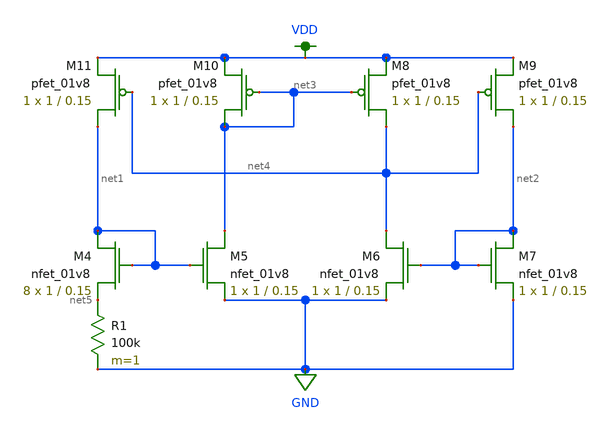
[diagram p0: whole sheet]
** sch_path: current_bias.sch
**.subckt current_bias
XM4 net1 net1 net5 GND sky130_fd_pr__nfet_01v8 L=0.15 W=1 nf=1 ad='int((nf+1)/2) * W/nf * 0.29' as='int((nf+2)/2) * W/nf * 0.29'
+ pd='2*int((nf+1)/2) * (W/nf + 0.29)' ps='2*int((nf+2)/2) * (W/nf + 0.29)' nrd='0.29 / W' nrs='0.29 / W'
+ sa=0 sb=0 sd=0 mult=8 m=8
XM5 net3 net1 GND GND sky130_fd_pr__nfet_01v8 L=0.15 W=1 nf=1 ad='int((nf+1)/2) * W/nf * 0.29' as='int((nf+2)/2) * W/nf * 0.29'
+ pd='2*int((nf+1)/2) * (W/nf + 0.29)' ps='2*int((nf+2)/2) * (W/nf + 0.29)' nrd='0.29 / W' nrs='0.29 / W'
+ sa=0 sb=0 sd=0 mult=1 m=1
XM6 net4 net2 GND GND sky130_fd_pr__nfet_01v8 L=0.15 W=1 nf=1 ad='int((nf+1)/2) * W/nf * 0.29' as='int((nf+2)/2) * W/nf * 0.29'
+ pd='2*int((nf+1)/2) * (W/nf + 0.29)' ps='2*int((nf+2)/2) * (W/nf + 0.29)' nrd='0.29 / W' nrs='0.29 / W'
+ sa=0 sb=0 sd=0 mult=1 m=1
XM7 net2 net2 GND GND sky130_fd_pr__nfet_01v8 L=0.15 W=1 nf=1 ad='int((nf+1)/2) * W/nf * 0.29' as='int((nf+2)/2) * W/nf * 0.29'
+ pd='2*int((nf+1)/2) * (W/nf + 0.29)' ps='2*int((nf+2)/2) * (W/nf + 0.29)' nrd='0.29 / W' nrs='0.29 / W'
+ sa=0 sb=0 sd=0 mult=1 m=1
R1 net5 GND 100k m=1
XM8 net4 net3 VDD VDD sky130_fd_pr__pfet_01v8 L=0.15 W=1 nf=1 ad='int((nf+1)/2) * W/nf * 0.29' as='int((nf+2)/2) * W/nf * 0.29'
+ pd='2*int((nf+1)/2) * (W/nf + 0.29)' ps='2*int((nf+2)/2) * (W/nf + 0.29)' nrd='0.29 / W' nrs='0.29 / W'
+ sa=0 sb=0 sd=0 mult=1 m=1
XM9 net2 net4 VDD VDD sky130_fd_pr__pfet_01v8 L=0.15 W=1 nf=1 ad='int((nf+1)/2) * W/nf * 0.29' as='int((nf+2)/2) * W/nf * 0.29'
+ pd='2*int((nf+1)/2) * (W/nf + 0.29)' ps='2*int((nf+2)/2) * (W/nf + 0.29)' nrd='0.29 / W' nrs='0.29 / W'
+ sa=0 sb=0 sd=0 mult=1 m=1
XM10 net3 net3 VDD VDD sky130_fd_pr__pfet_01v8 L=0.15 W=1 nf=1 ad='int((nf+1)/2) * W/nf * 0.29' as='int((nf+2)/2) * W/nf * 0.29'
+ pd='2*int((nf+1)/2) * (W/nf + 0.29)' ps='2*int((nf+2)/2) * (W/nf + 0.29)' nrd='0.29 / W' nrs='0.29 / W'
+ sa=0 sb=0 sd=0 mult=1 m=1
XM11 net1 net4 VDD VDD sky130_fd_pr__pfet_01v8 L=0.15 W=1 nf=1 ad='int((nf+1)/2) * W/nf * 0.29' as='int((nf+2)/2) * W/nf * 0.29'
+ pd='2*int((nf+1)/2) * (W/nf + 0.29)' ps='2*int((nf+2)/2) * (W/nf + 0.29)' nrd='0.29 / W' nrs='0.29 / W'
+ sa=0 sb=0 sd=0 mult=1 m=1
**.ends
.GLOBAL VDD
.GLOBAL GND
.end
